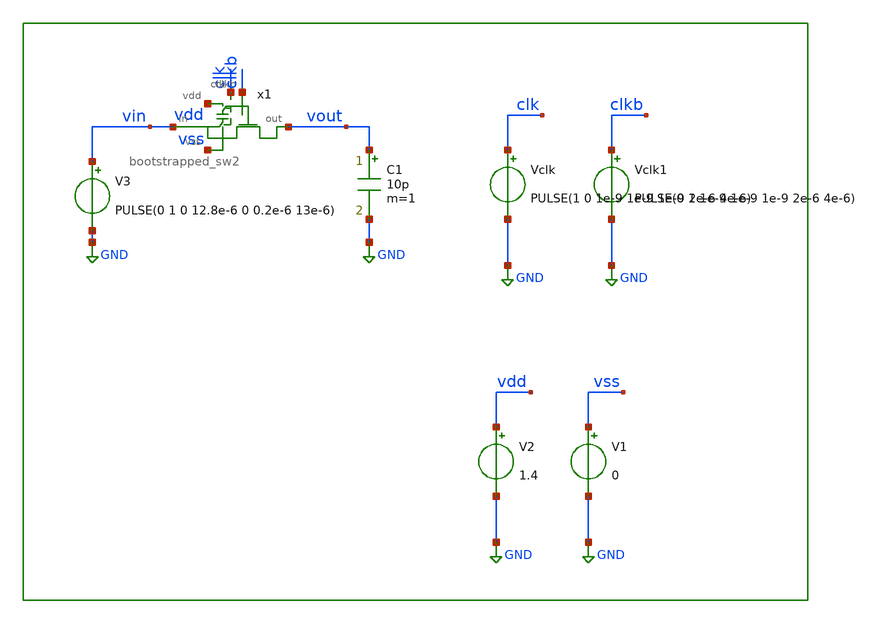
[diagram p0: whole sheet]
** sch_path: xschem/tb/switches/tr_bootstrapped_sw.sch
**.subckt tr_bootstrapped_sw
V1 vss GND 0
V2 vdd GND 1.4
Vclk clk GND PULSE(1 0 1e-9 1e-9 1e-9 2e-6 4e-6)
C1 vout GND 10p m=1
V3 vin GND PULSE(0 1 0 12.8e-6 0 0.2e-6 13e-6)
x1 clkb vout clk vdd vin vss bootstrapped_sw2
Vclk1 clkb GND PULSE(0 1 1e-9 1e-9 1e-9 2e-6 4e-6)
**** begin user architecture code
 *.options method trap
*.options gmin 1e-15
*.options abstol 1e-15
*.options reltol 0.0001
*.options vntol 0.1e-6
*
.include $::DESIGN_PATH/switches/bootstrapped_sw.sp


.param MC_SWITCH=0

*.tran 100e-9 4e-6
.temp 85

.control
save all
tran 100e-9 13e-6 uic
run


* settle values
meas tran vset find v(vout) at=3.99e-6
meas tran vg_end find v(xsw.vg) at=3.99e-6
meas tran vin_end find v(vin) at=3.99e-6

let vgs_end=vg_end-vin_end

* max values
meas tran vg_max max xsw.vg
meas tran vs_max max xsw.vs
meas tran vbsl_max max xsw.vbsl
meas tran vbsh_max max xsw.vbsh

* min values
meas tran vg_min min xsw.vg
meas tran vs_min min xsw.vs
meas tran vbsl_min min xsw.vbsl
meas tran vbsh_min min xsw.vbsh


* print results
print vset
print vgs_end

print vg_max
print vs_max
print vbsl_max
print vbsh_max
print vg_min
print vs_min
print vbsl_min
print vbsh_min

.endc

 * FET CORNERS
.include $::SKYWATER_MODELS/models/corners/tt.spice
*.include $::SKYWATER_MODELS//corners/ff.spice
*.include $::SKYWATER_MODELS/corners/ss.spice
*.include $::SKYWATER_MODELS/corners/sf.spice
*.include $::SKYWATER_MODELS/corners/fs.spice

* TT + R + C
*.include $::SKYWATER_MODELS/corners/tt_rmax_cmax.spice
*.include $::SKYWATER_MODELS/corners/tt_rmin_cmin.spice
*.include $::SKYWATER_MODELS/corners/tt_rmax_cmin.spice
*.include $::SKYWATER_MODELS/corners/tt_rmin_cmax.spice

* FF + R + C
*.include $::SKYWATER_MODELS/corners/ff_rmax_cmax.spice
*.include $::SKYWATER_MODELS/corners/ff_rmin_cmin.spice
*.include $::SKYWATER_MODELS/corners/ff_rmax_cmin.spice
*.include $::SKYWATER_MODELS/corners/ff_rmin_cmax.spice


* SS + R + C
*.include $::SKYWATER_MODELS/corners/ss_rmax_cmax.spice
*.include $::SKYWATER_MODELS/corners/ss_rmin_cmin.spice
*.include $::SKYWATER_MODELS/corners/ss_rmax_cmin.spice
*.include $::SKYWATER_MODELS/corners/ss_rmin_cmax.spice

* SF + R + C
*.include $::SKYWATER_MODELS/corners/sf_rmax_cmax.spice
*.include $::SKYWATER_MODELS/corners/sf_rmin_cmin.spice
*.include $::SKYWATER_MODELS/corners/sf_rmax_cmin.spice
*.include $::SKYWATER_MODELS/corners/sf_rmin_cmax.spice

* FS + R + C
*.include $::SKYWATER_MODELS/corners/fs_rmax_cmax.spice
*.include $::SKYWATER_MODELS/corners/fs_rmin_cmin.spice
*.include $::SKYWATER_MODELS/corners/fs_rmax_cmin.spice
*.include $::SKYWATER_MODELS/corners/fs_rmin_cmax.spice

**** end user architecture code
**.ends
.GLOBAL GND
.end
